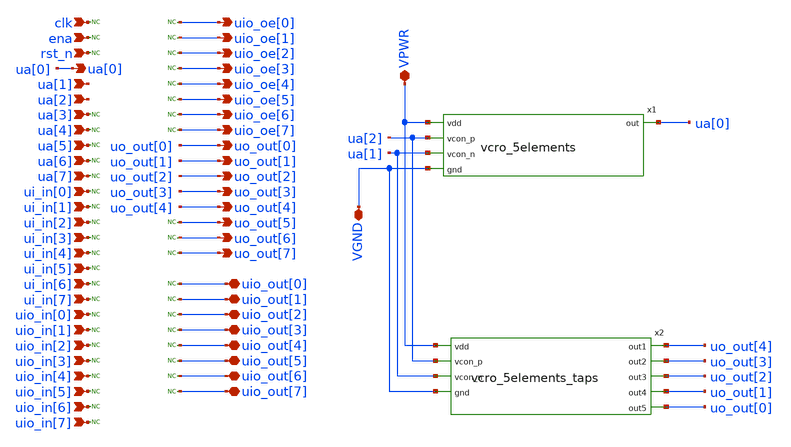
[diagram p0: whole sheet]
** sch_path: xschem/tt_um_nurirfansyah_alits01.sch
**.subckt tt_um_nurirfansyah_alits01 clk ena rst_n ua[3] ua[4] ua[5] ua[6] ua[7] ui_in[1] ui_in[2]
*+ ui_in[3] ui_in[4] ui_in[5] ui_in[6] ui_in[7] uio_in[0] uio_in[1] uio_in[2] uio_in[3] uio_in[4] uio_in[5]
*+ uio_in[6] uio_in[7] uio_oe[0] uio_oe[1] uio_oe[2] uio_oe[3] uio_oe[4] uio_oe[5] uio_oe[6] uio_oe[7] uo_out[1]
*+ uo_out[2] uo_out[3] uo_out[4] uo_out[5] uo_out[6] uo_out[7] uio_out[0] uio_out[1] uio_out[2] uio_out[3]
*+ uio_out[4] uio_out[5] uio_out[6] uio_out[7] ua[2] ua[1] ui_in[0] uo_out[0] ua[0] VGND VPWR
*.ipin clk
*.ipin ena
*.ipin rst_n
*.ipin ua[3]
*.ipin ua[4]
*.ipin ua[5]
*.ipin ua[6]
*.ipin ua[7]
*.ipin ui_in[1]
*.ipin ui_in[2]
*.ipin ui_in[3]
*.ipin ui_in[4]
*.ipin ui_in[5]
*.ipin ui_in[6]
*.ipin ui_in[7]
*.ipin uio_in[0]
*.ipin uio_in[1]
*.ipin uio_in[2]
*.ipin uio_in[3]
*.ipin uio_in[4]
*.ipin uio_in[5]
*.ipin uio_in[6]
*.ipin uio_in[7]
*.opin uio_oe[0]
*.opin uio_oe[1]
*.opin uio_oe[2]
*.opin uio_oe[3]
*.opin uio_oe[4]
*.opin uio_oe[5]
*.opin uio_oe[6]
*.opin uio_oe[7]
*.opin uo_out[1]
*.opin uo_out[2]
*.opin uo_out[3]
*.opin uo_out[4]
*.opin uo_out[5]
*.opin uo_out[6]
*.opin uo_out[7]
*.iopin uio_out[0]
*.iopin uio_out[1]
*.iopin uio_out[2]
*.iopin uio_out[3]
*.iopin uio_out[4]
*.iopin uio_out[5]
*.iopin uio_out[6]
*.iopin uio_out[7]
*.ipin ua[2]
*.ipin ua[1]
*.ipin ui_in[0]
*.opin uo_out[0]
*.opin ua[0]
*.iopin VGND
*.iopin VPWR
* noconn clk
* noconn ena
* noconn rst_n
* noconn ua[3]
* noconn ua[6]
* noconn ui_in[1]
* noconn ui_in[2]
* noconn ui_in[3]
* noconn ui_in[4]
* noconn ui_in[5]
* noconn ui_in[6]
* noconn ui_in[7]
* noconn uio_in[0]
* noconn uio_in[1]
* noconn uio_in[2]
* noconn uio_in[3]
* noconn uio_in[4]
* noconn uio_in[5]
* noconn uio_in[6]
* noconn uio_in[7]
* noconn ua[5]
* noconn ua[4]
* noconn ua[7]
* noconn ui_in[0]
x1 ua[0] VPWR ua[2] ua[1] VGND vcro_5elements
* noconn uio_oe[0]
* noconn uio_oe[1]
* noconn uio_oe[2]
* noconn uio_oe[3]
* noconn uio_oe[4]
* noconn uio_oe[5]
* noconn uio_oe[6]
* noconn uio_oe[7]
* noconn uo_out[5]
* noconn uo_out[6]
* noconn uo_out[7]
* noconn uio_out[0]
* noconn uio_out[1]
* noconn uio_out[2]
* noconn uio_out[3]
* noconn uio_out[4]
* noconn uio_out[5]
* noconn uio_out[6]
* noconn uio_out[7]
x2 uo_out[4] uo_out[3] uo_out[2] uo_out[1] uo_out[0] VPWR ua[2] ua[1] VGND vcro_5elements_taps
**.ends
.end
